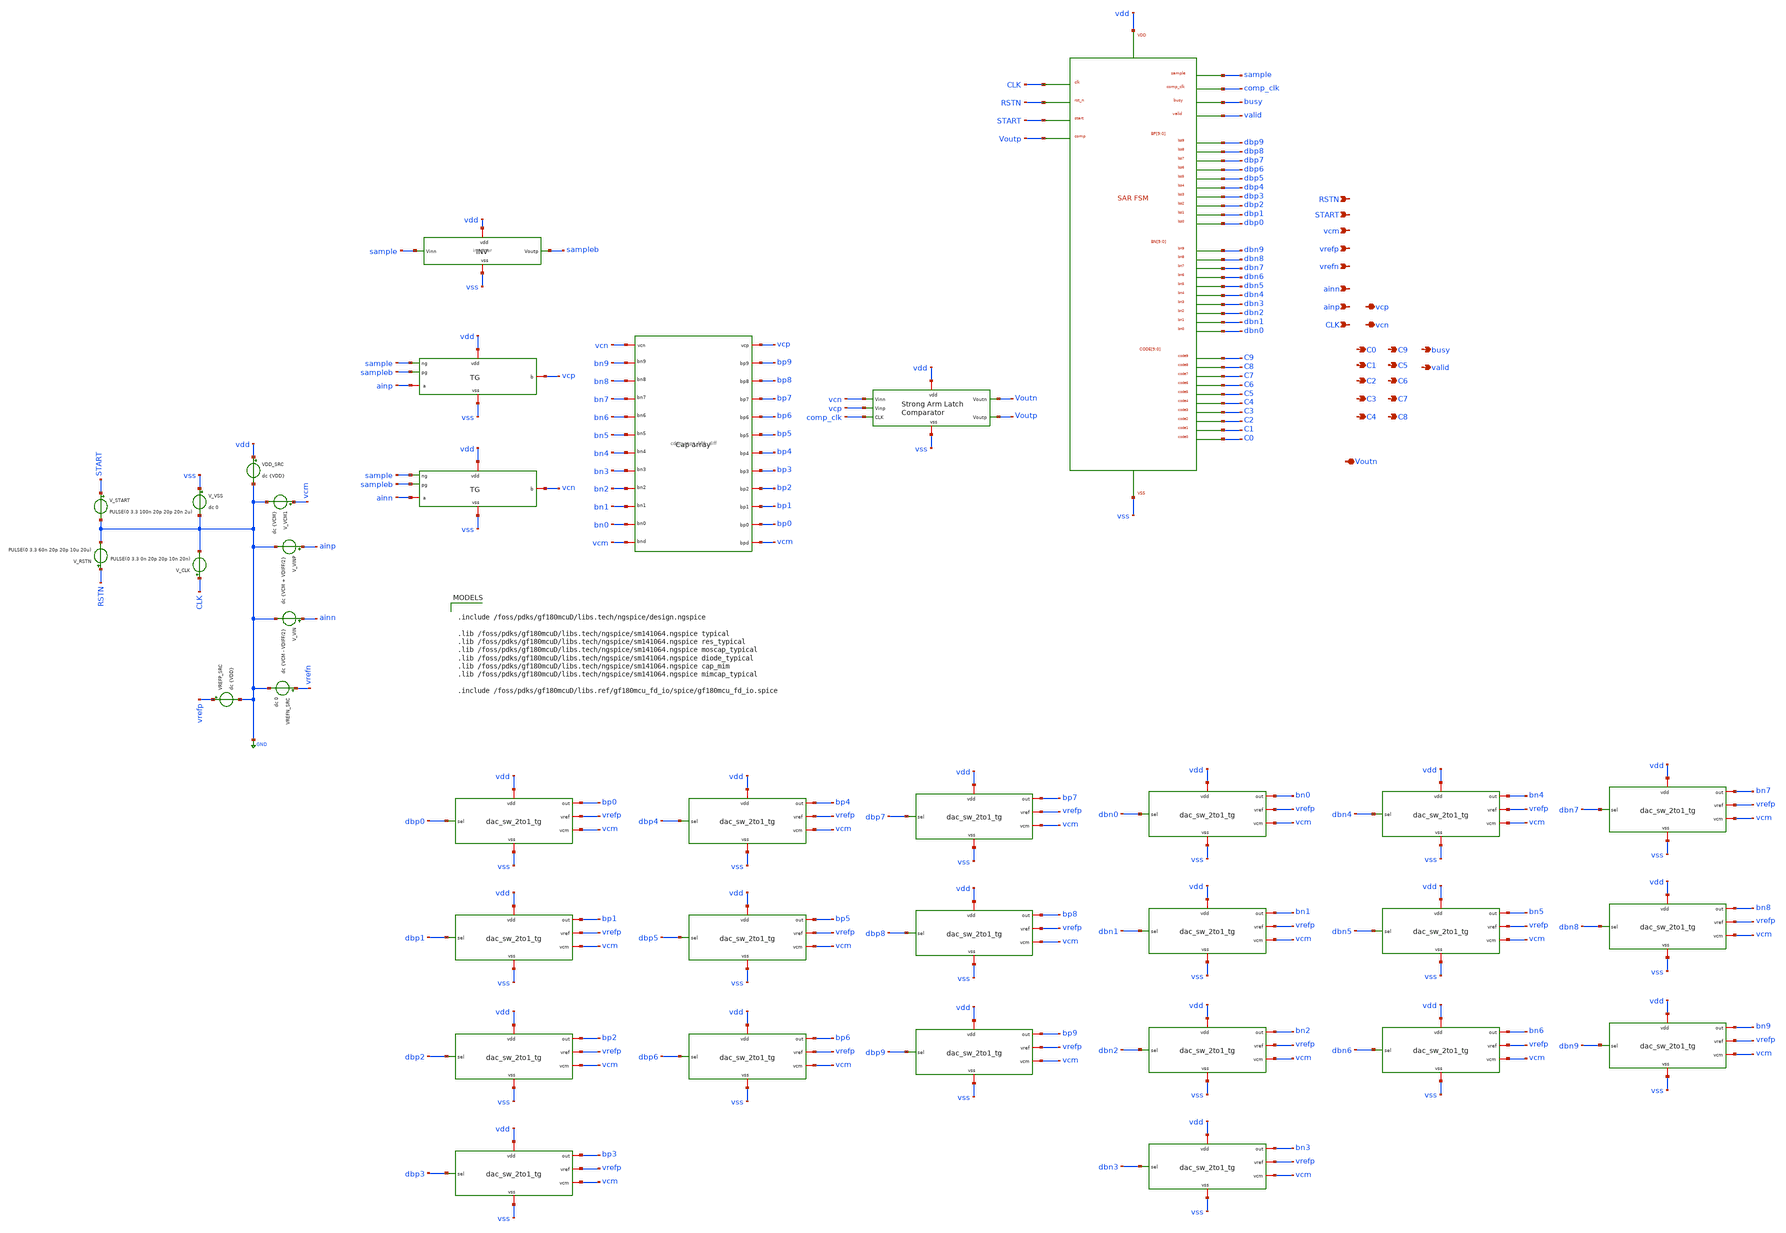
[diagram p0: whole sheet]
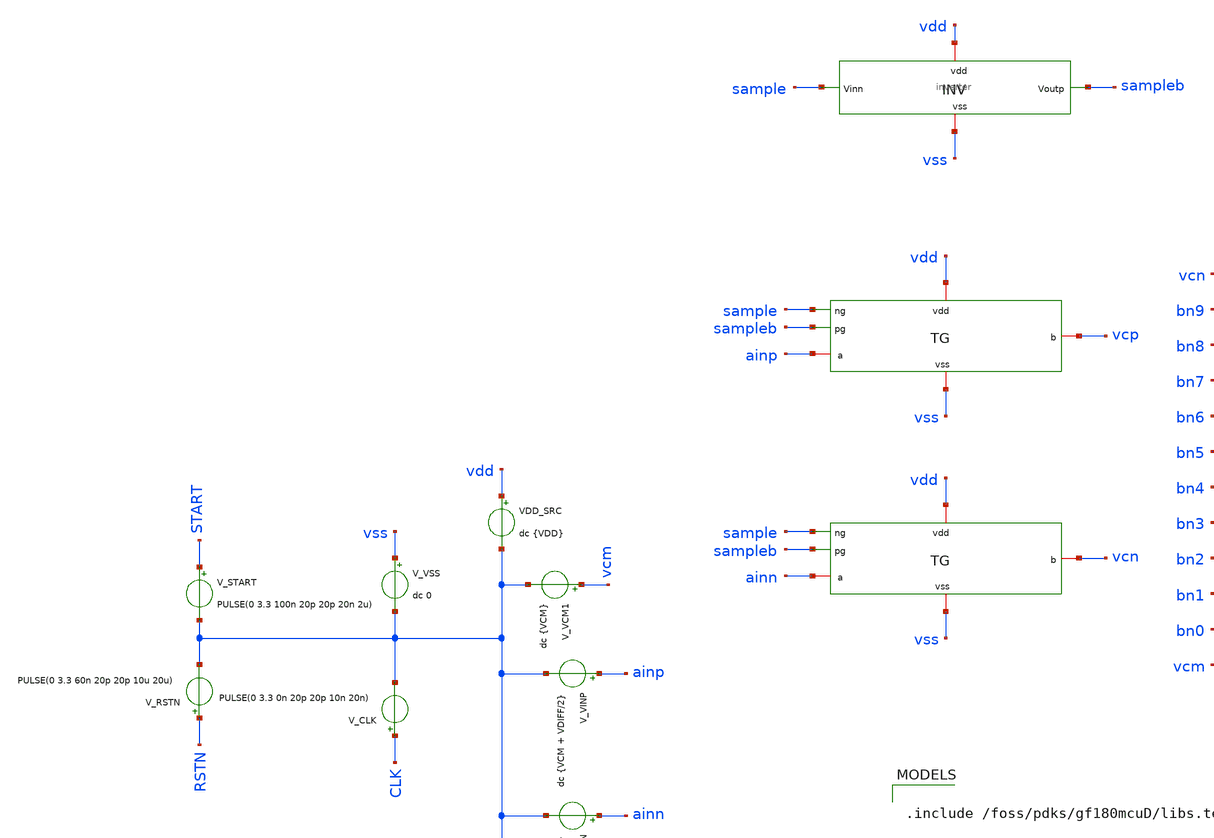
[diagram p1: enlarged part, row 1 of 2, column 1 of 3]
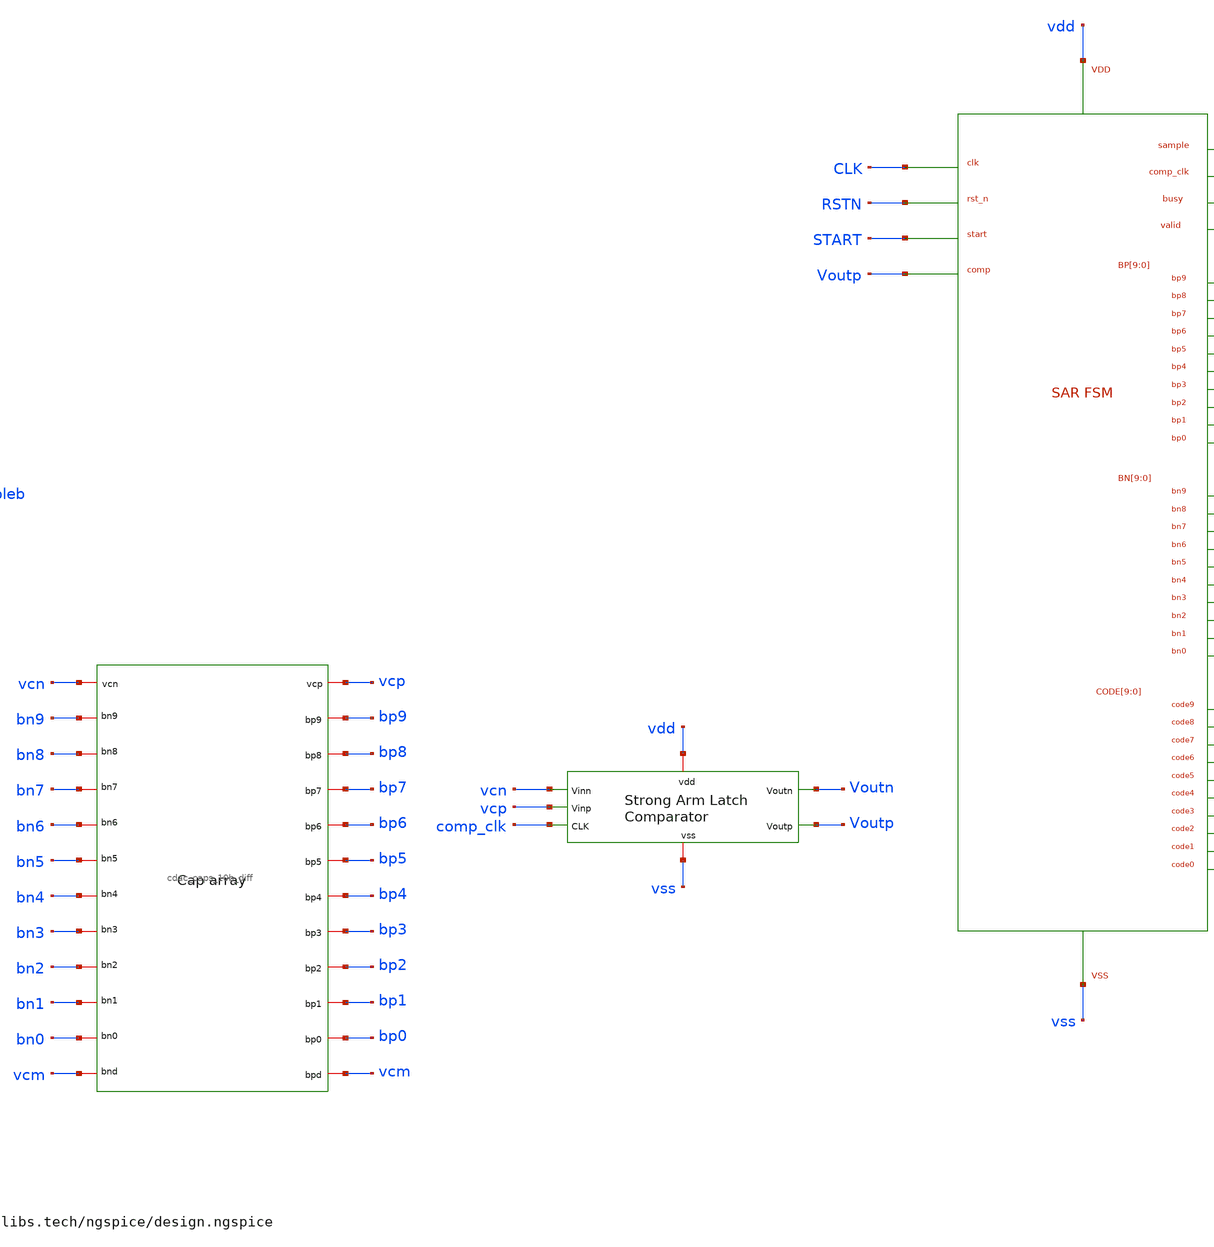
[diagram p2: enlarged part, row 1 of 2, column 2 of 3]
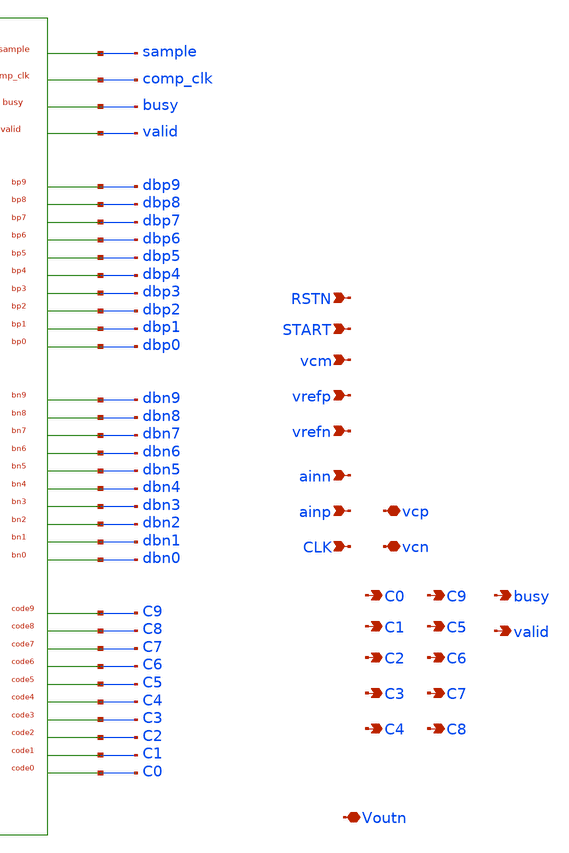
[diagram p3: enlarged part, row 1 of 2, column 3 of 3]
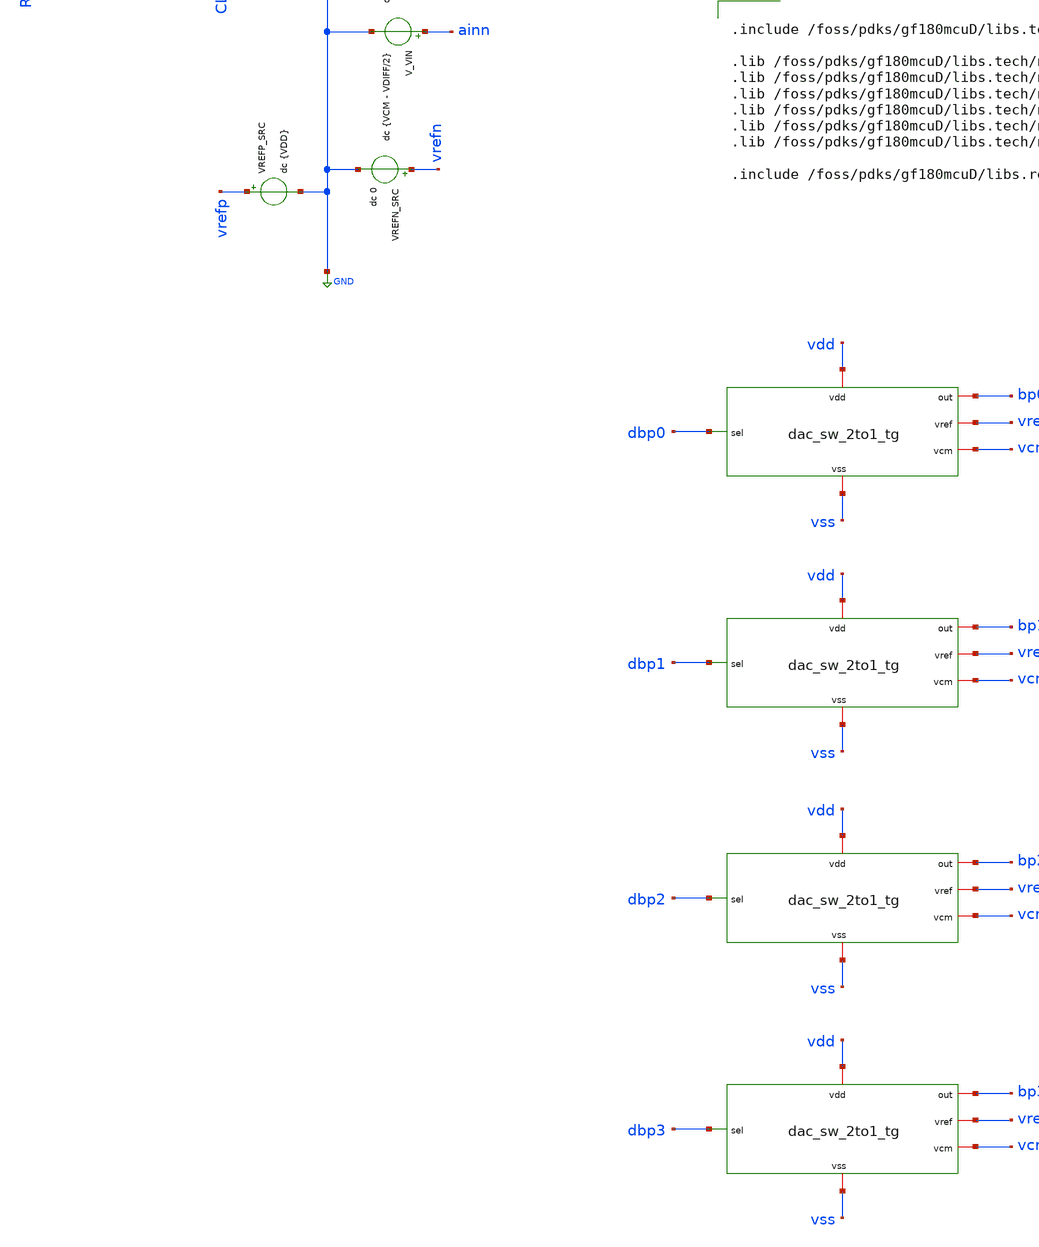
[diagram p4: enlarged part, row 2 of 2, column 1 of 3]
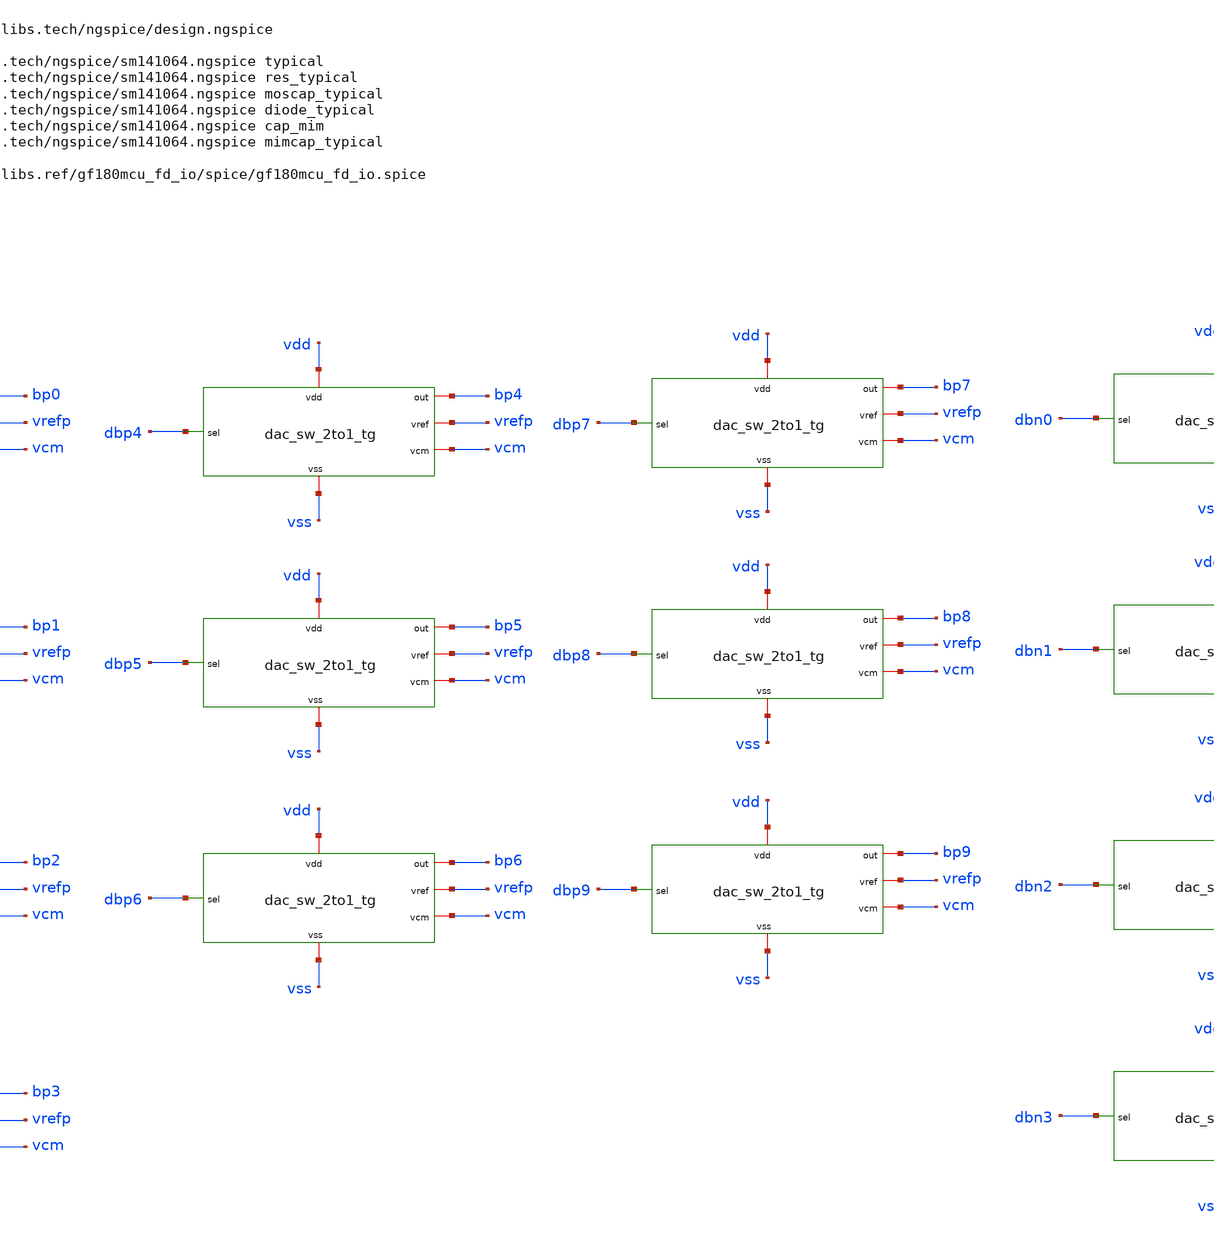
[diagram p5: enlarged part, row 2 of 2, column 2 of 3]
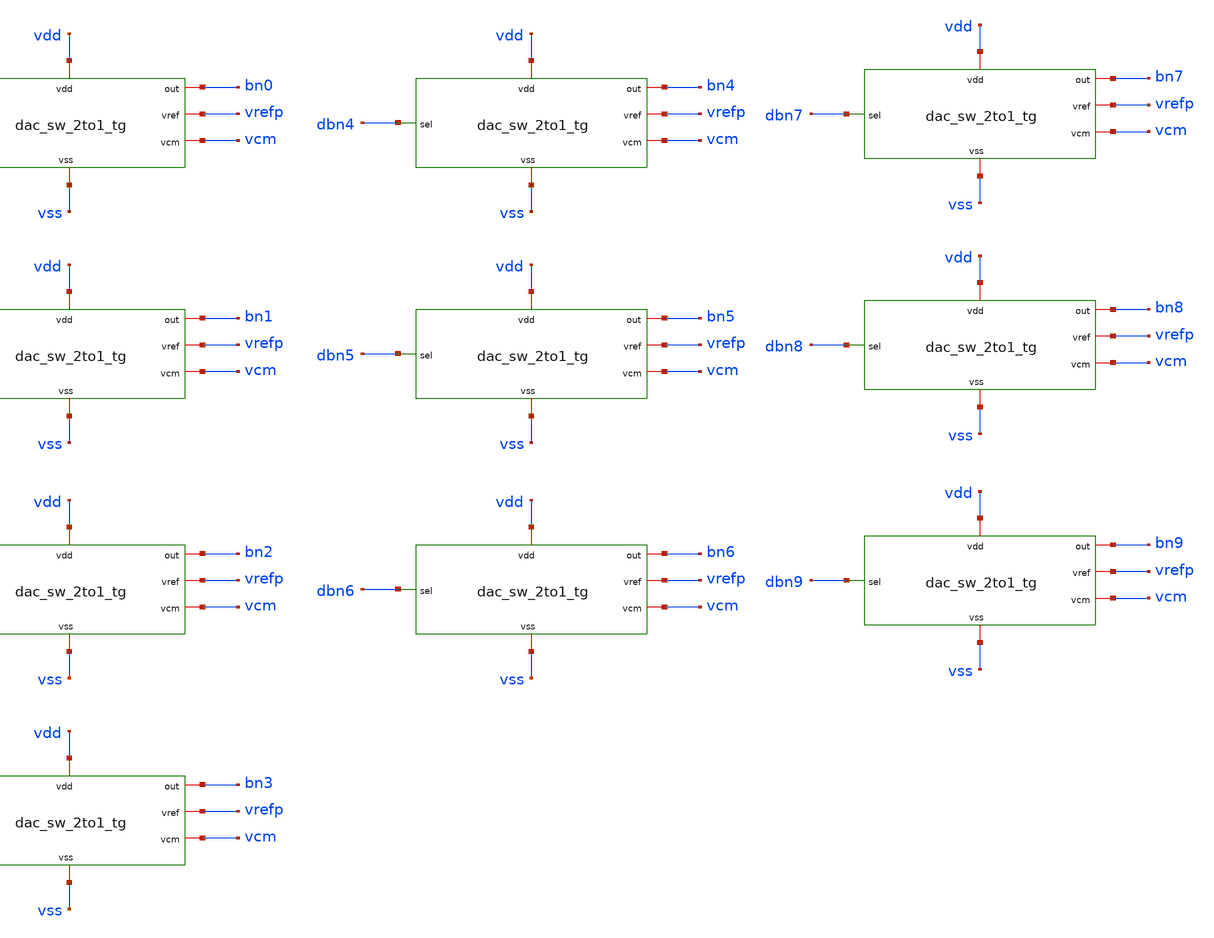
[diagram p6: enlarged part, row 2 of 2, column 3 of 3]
** sch_path: circuit_files/sar_adc_test/tb/cdac_comp_sar_fsm_tb.sch
**.subckt cdac_comp_sar_fsm_tb ainn vcp ainp CLK vcn vrefp vrefn vcm C1 C2 C3 C4 C5 C6 C7 C8 C0 C9
*+ busy valid START RSTN Voutn
*.ipin ainn
*.iopin vcp
*.ipin ainp
*.ipin CLK
*.iopin vcn
*.ipin vrefp
*.ipin vrefn
*.ipin vcm
*.opin C1
*.opin C2
*.opin C3
*.opin C4
*.opin C5
*.opin C6
*.opin C7
*.opin C8
*.opin C0
*.opin C9
*.opin busy
*.opin valid
*.ipin START
*.ipin RSTN
*.iopin Voutn
V_VIN ainn GND dc {VCM - VDIFF/2}
VDD_SRC vdd GND dc {VDD}
V_VINP ainp GND dc {VCM + VDIFF/2}
V_VSS vss GND dc 0
V_CLK CLK GND PULSE(0 3.3 0n 20p 20p 10n 20n)
x1 Voutn vcn Voutp vcp vdd vss comp_clk strong_arm_comp
x3 vss sample sampleb vdd ainp vcp tg
x4 vss sample sampleb vdd ainn vcn tg
V_VCM1 vcm GND dc {VCM}
x2 vcp bp3 bp0 bp5 bp2 vcm bp1 bp7 bp6 bp8 bp4 bp9 vcn bn0 bn1 bn8 bn7 bn6 bn5 bn4 bn3 bn9 bn2 vcm
+ cdac_caps_10b_diff
VREFN_SRC vrefn GND dc 0
VREFP_SRC vrefp GND dc {VDD}
V_RSTN RSTN GND PULSE(0 3.3 60n 20p 20p 10u 20u)
V_START START GND PULSE(0 3.3 100n 20p 20p 20n 2u)
x6 dbp0 bp0 vss vdd vrefp vcm dac_sw_2to1_tg
x7 dbp1 bp1 vss vdd vrefp vcm dac_sw_2to1_tg
x8 dbp4 bp4 vss vdd vrefp vcm dac_sw_2to1_tg
x9 dbp5 bp5 vss vdd vrefp vcm dac_sw_2to1_tg
x10 dbp7 bp7 vss vdd vrefp vcm dac_sw_2to1_tg
x11 dbp8 bp8 vss vdd vrefp vcm dac_sw_2to1_tg
x12 dbp2 bp2 vss vdd vrefp vcm dac_sw_2to1_tg
x13 dbp3 bp3 vss vdd vrefp vcm dac_sw_2to1_tg
x14 dbp6 bp6 vss vdd vrefp vcm dac_sw_2to1_tg
x16 dbp9 bp9 vss vdd vrefp vcm dac_sw_2to1_tg
x17 dbn0 bn0 vss vdd vrefp vcm dac_sw_2to1_tg
x18 dbn1 bn1 vss vdd vrefp vcm dac_sw_2to1_tg
x19 dbn4 bn4 vss vdd vrefp vcm dac_sw_2to1_tg
x20 dbn5 bn5 vss vdd vrefp vcm dac_sw_2to1_tg
x21 dbn7 bn7 vss vdd vrefp vcm dac_sw_2to1_tg
x22 dbn8 bn8 vss vdd vrefp vcm dac_sw_2to1_tg
x23 dbn2 bn2 vss vdd vrefp vcm dac_sw_2to1_tg
x24 dbn3 bn3 vss vdd vrefp vcm dac_sw_2to1_tg
x25 dbn6 bn6 vss vdd vrefp vcm dac_sw_2to1_tg
x27 dbn9 bn9 vss vdd vrefp vcm dac_sw_2to1_tg
x15 vdd sample sampleb vss inverter
x26 CLK RSTN START Voutp sample comp_clk busy valid dbp9 dbp8 dbp7 dbp6 dbp5 dbp4 dbp3 dbp2 dbp1
+ dbp0 dbn9 dbn8 dbn7 dbn6 dbn5 dbn4 dbn3 dbn2 dbn1 dbn0 C9 C8 C7 C6 C5 C4 C3 C2 C1 C0 vdd vss
+ sar_fsm_wrapper
**** begin user architecture code

.include /foss/pdks/gf180mcuD/libs.tech/ngspice/design.ngspice

.lib /foss/pdks/gf180mcuD/libs.tech/ngspice/sm141064.ngspice typical
.lib /foss/pdks/gf180mcuD/libs.tech/ngspice/sm141064.ngspice res_typical
.lib /foss/pdks/gf180mcuD/libs.tech/ngspice/sm141064.ngspice moscap_typical
.lib /foss/pdks/gf180mcuD/libs.tech/ngspice/sm141064.ngspice diode_typical
.lib /foss/pdks/gf180mcuD/libs.tech/ngspice/sm141064.ngspice cap_mim
.lib /foss/pdks/gf180mcuD/libs.tech/ngspice/sm141064.ngspice mimcap_typical

.include /foss/pdks/gf180mcuD/libs.ref/gf180mcu_fd_io/spice/gf180mcu_fd_io.spice



* ============================================================
* GF180 / SAR FSM + Comparator + CDAC mixed-signal testbench
* REAL DAC-switch version
* ============================================================

* Standard-cell SPICE and SAR FSM wrapper
.include /foss/pdks/gf180mcuD/libs.ref/gf180mcu_fd_sc_mcu7t5v0/spice/gf180mcu_fd_sc_mcu7t5v0.spice
.include /media/sf_LNA_chipathon/OCCPSense_Capacitive_Pressure_Sensor/rtl/sar_fsm/sar_fsm_wrapper_fixed.spice

* ------------------------------------------------------------
* Main parameters
* ------------------------------------------------------------
.param VDD=3.3
.param VCM=1.65
.param VDIFF=0.001611328125
.param WCU=5u
.param LCU=5u
.param COUT_LOAD=20f


* ============================================================
* SAR ADC POST-FIX SMALL RAMP DEBUG
* Dumps one row per VDIFF into:
*   sar_ramp_after_fix_results.txt
*
* Assumes current fixed schematic:
*   BP-side DAC vref pin -> vrefp
*   BN-side DAC vref pin -> vrefp
* ============================================================

.options reltol=1e-4 abstol=1e-12 vntol=1e-6
.options method=gear maxord=2
.options plotwinsize=0

* -----------------------------
* Save required nodes
* -----------------------------
.save v(CLK) v(RSTN) v(START)
.save v(sample) v(sampleb) v(comp_clk)
.save v(busy) v(valid)

.save v(ainp) v(ainn)
.save v(vcp) v(vcn)
.save v(vrefp) v(vrefn) v(vcm)
.save v(Voutp) v(Voutn)

.save v(C9) v(C8) v(C7) v(C6) v(C5)
.save v(C4) v(C3) v(C2) v(C1) v(C0)

.save v(dbp9) v(dbp8) v(dbp7) v(dbp6) v(dbp5)
.save v(dbp4) v(dbp3) v(dbp2) v(dbp1) v(dbp0)

.save v(dbn9) v(dbn8) v(dbn7) v(dbn6) v(dbn5)
.save v(dbn4) v(dbn3) v(dbn2) v(dbn1) v(dbn0)

.save v(bp9) v(bp8) v(bp7) v(bp6) v(bp5)
.save v(bp4) v(bp3) v(bp2) v(bp1) v(bp0)

.save v(bn9) v(bn8) v(bn7) v(bn6) v(bn5)
.save v(bn4) v(bn3) v(bn2) v(bn1) v(bn0)

.control

set noaskquit

shell rm -f sar_ramp_after_fix_results.txt

let logic_th = 1.65
let prev_code = -1
let run_index = 0
let monotonic_fail_count = 0

echo VDIFF VALID_SEEN T_DEBUG CODE C9 C8 C7 C6 C5 C4 C3 C2 C1 C0 VCP VCN VCP_MINUS_VCN VOUTP VOUTN
+ DBP9 DBP8 DBP7 DBP6 DBP5 DBP4 DBP3 DBP2 DBP1 DBP0 DBN9 DBN8 DBN7 DBN6 DBN5 DBN4 DBN3 DBN2 DBN1 DBN0 BP9
+ BP8 BP7 BP6 BP5 BP4 BP3 BP2 BP1 BP0 BN9 BN8 BN7 BN6 BN5 BN4 BN3 BN2 BN1 BN0 MONOTONIC_FAIL >
+ sar_ramp_after_fix_results.txt

* Small ramp around midscale.
foreach vdiff_val -0.020 -0.010 -0.005 -0.002 -0.001 0 0.001 0.001611328125 0.002 0.005 0.010 0.020

  alterparam VDIFF = $vdiff_val
  reset

  tran 20p 1.6u

  meas tran valid_max MAX v(valid) FROM=0n TO=1.6u

  let valid_seen = 0
  if valid_max > logic_th
    let valid_seen = 1
  end

  let t_debug = 1.55u
  if valid_seen > 0.5
    meas tran t_valid WHEN v(valid)=1.65 RISE=1
    let t_debug = t_valid + 5n
  end

  * -----------------------------
  * Code bits at debug time
  * -----------------------------
  meas tran c9v FIND v(C9) AT=$&t_debug
  meas tran c8v FIND v(C8) AT=$&t_debug
  meas tran c7v FIND v(C7) AT=$&t_debug
  meas tran c6v FIND v(C6) AT=$&t_debug
  meas tran c5v FIND v(C5) AT=$&t_debug
  meas tran c4v FIND v(C4) AT=$&t_debug
  meas tran c3v FIND v(C3) AT=$&t_debug
  meas tran c2v FIND v(C2) AT=$&t_debug
  meas tran c1v FIND v(C1) AT=$&t_debug
  meas tran c0v FIND v(C0) AT=$&t_debug

  let b9 = 0
  if c9v > logic_th
    let b9 = 1
  end

  let b8 = 0
  if c8v > logic_th
    let b8 = 1
  end

  let b7 = 0
  if c7v > logic_th
    let b7 = 1
  end

  let b6 = 0
  if c6v > logic_th
    let b6 = 1
  end

  let b5 = 0
  if c5v > logic_th
    let b5 = 1
  end

  let b4 = 0
  if c4v > logic_th
    let b4 = 1
  end

  let b3 = 0
  if c3v > logic_th
    let b3 = 1
  end

  let b2 = 0
  if c2v > logic_th
    let b2 = 1
  end

  let b1 = 0
  if c1v > logic_th
    let b1 = 1
  end

  let b0 = 0
  if c0v > logic_th
    let b0 = 1
  end

  let adc_code = 512*b9 + 256*b8 + 128*b7 + 64*b6 + 32*b5 + 16*b4 + 8*b3 + 4*b2 + 2*b1 + b0

  * -----------------------------
  * Analog values
  * -----------------------------
  meas tran vcpv   FIND v(vcp)   AT=$&t_debug
  meas tran vcnv   FIND v(vcn)   AT=$&t_debug
  meas tran voutpv FIND v(Voutp) AT=$&t_debug
  meas tran voutnv FIND v(Voutn) AT=$&t_debug

  let vdiff_cdac = vcpv - vcnv

  * -----------------------------
  * SAR DAC digital controls
  * -----------------------------
  meas tran dbp9v FIND v(dbp9) AT=$&t_debug
  meas tran dbp8v FIND v(dbp8) AT=$&t_debug
  meas tran dbp7v FIND v(dbp7) AT=$&t_debug
  meas tran dbp6v FIND v(dbp6) AT=$&t_debug
  meas tran dbp5v FIND v(dbp5) AT=$&t_debug
  meas tran dbp4v FIND v(dbp4) AT=$&t_debug
  meas tran dbp3v FIND v(dbp3) AT=$&t_debug
  meas tran dbp2v FIND v(dbp2) AT=$&t_debug
  meas tran dbp1v FIND v(dbp1) AT=$&t_debug
  meas tran dbp0v FIND v(dbp0) AT=$&t_debug

  meas tran dbn9v FIND v(dbn9) AT=$&t_debug
  meas tran dbn8v FIND v(dbn8) AT=$&t_debug
  meas tran dbn7v FIND v(dbn7) AT=$&t_debug
  meas tran dbn6v FIND v(dbn6) AT=$&t_debug
  meas tran dbn5v FIND v(dbn5) AT=$&t_debug
  meas tran dbn4v FIND v(dbn4) AT=$&t_debug
  meas tran dbn3v FIND v(dbn3) AT=$&t_debug
  meas tran dbn2v FIND v(dbn2) AT=$&t_debug
  meas tran dbn1v FIND v(dbn1) AT=$&t_debug
  meas tran dbn0v FIND v(dbn0) AT=$&t_debug

  * -----------------------------
  * Actual CDAC bottom plates
  * -----------------------------
  meas tran bp9v FIND v(bp9) AT=$&t_debug
  meas tran bp8v FIND v(bp8) AT=$&t_debug
  meas tran bp7v FIND v(bp7) AT=$&t_debug
  meas tran bp6v FIND v(bp6) AT=$&t_debug
  meas tran bp5v FIND v(bp5) AT=$&t_debug
  meas tran bp4v FIND v(bp4) AT=$&t_debug
  meas tran bp3v FIND v(bp3) AT=$&t_debug
  meas tran bp2v FIND v(bp2) AT=$&t_debug
  meas tran bp1v FIND v(bp1) AT=$&t_debug
  meas tran bp0v FIND v(bp0) AT=$&t_debug

  meas tran bn9v FIND v(bn9) AT=$&t_debug
  meas tran bn8v FIND v(bn8) AT=$&t_debug
  meas tran bn7v FIND v(bn7) AT=$&t_debug
  meas tran bn6v FIND v(bn6) AT=$&t_debug
  meas tran bn5v FIND v(bn5) AT=$&t_debug
  meas tran bn4v FIND v(bn4) AT=$&t_debug
  meas tran bn3v FIND v(bn3) AT=$&t_debug
  meas tran bn2v FIND v(bn2) AT=$&t_debug
  meas tran bn1v FIND v(bn1) AT=$&t_debug
  meas tran bn0v FIND v(bn0) AT=$&t_debug

  * -----------------------------
  * Monotonic check
  * -----------------------------
  let monotonic_fail = 0
  if run_index > 0
    if adc_code < prev_code
      let monotonic_fail = 1
      let monotonic_fail_count = monotonic_fail_count + 1
    end
  end

  echo $vdiff_val $&valid_seen $&t_debug $&adc_code $&b9 $&b8 $&b7 $&b6 $&b5 $&b4 $&b3 $&b2 $&b1
+ $&b0 $&vcpv $&vcnv $&vdiff_cdac $&voutpv $&voutnv $&dbp9v $&dbp8v $&dbp7v $&dbp6v $&dbp5v $&dbp4v
+ $&dbp3v $&dbp2v $&dbp1v $&dbp0v $&dbn9v $&dbn8v $&dbn7v $&dbn6v $&dbn5v $&dbn4v $&dbn3v $&dbn2v $&dbn1v
+ $&dbn0v $&bp9v $&bp8v $&bp7v $&bp6v $&bp5v $&bp4v $&bp3v $&bp2v $&bp1v $&bp0v $&bn9v $&bn8v $&bn7v $&bn6v
+ $&bn5v $&bn4v $&bn3v $&bn2v $&bn1v $&bn0v $&monotonic_fail >> sar_ramp_after_fix_results.txt

  let prev_code = adc_code
  let run_index = run_index + 1

end

echo ================================================== >> sar_ramp_after_fix_results.txt
echo RAMP_SUMMARY >> sar_ramp_after_fix_results.txt
echo number_of_points = $&run_index >> sar_ramp_after_fix_results.txt
echo monotonic_fail_count = $&monotonic_fail_count >> sar_ramp_after_fix_results.txt
echo Expected_after_fix: code should move monotonically with VDIFF. >>
+ sar_ramp_after_fix_results.txt
echo Near VDIFF=0, code should be close to 511 or 512. >> sar_ramp_after_fix_results.txt
echo ================================================== >> sar_ramp_after_fix_results.txt

echo ==================================================
echo SAR post-fix ramp test complete.
echo Results written to sar_ramp_after_fix_results.txt
echo ==================================================

.endc



**** end user architecture code
**.ends

* expanding   symbol:  strong_arm_comp.sym # of pins=7
** sym_path: circuit_files/sar_adc_test/xschem/strong_arm_comp.sym
** sch_path: circuit_files/sar_adc_test/xschem/strong_arm_comp.sch
.subckt strong_arm_comp Voutn Vinn Voutp Vinp vdd vss CLK
*.ipin Vinn
*.opin Voutp
*.iopin vdd
*.ipin Vinp
*.ipin CLK
*.iopin vss
*.opin Voutn
XM1 P CLK vdd vdd sg13_hv_pmos w=2u l=0.4u ng=1 m=4 mm_ok=1
XM2 net1 CLK vss vss sg13_hv_nmos w=2u l=0.45u ng=1 m=8 mm_ok=1
XM3 X CLK vdd vdd sg13_hv_pmos w=2u l=0.4u ng=1 m=4 mm_ok=1
XM4 P Vinn net1 vss sg13_hv_nmos w=2u l=0.45u ng=1 m=6 mm_ok=1
XM5 Q Vinp net1 vss sg13_hv_nmos w=2u l=0.45u ng=1 m=6 mm_ok=1
XM6 X Y P vss sg13_hv_nmos w=2u l=0.45u ng=1 m=2 mm_ok=1
XM7 Y X Q vss sg13_hv_nmos w=2u l=0.45u ng=1 m=2 mm_ok=1
XM8 X Y vdd vdd sg13_hv_pmos w=2u l=0.4u ng=1 m=4 mm_ok=1
XM9 Y CLK vdd vdd sg13_hv_pmos w=2u l=0.4u ng=1 m=4 mm_ok=1
XM10 Q CLK vdd vdd sg13_hv_pmos w=2u l=0.4u ng=1 m=4 mm_ok=1
XM11 Y X vdd vdd sg13_hv_pmos w=2u l=0.4u ng=1 m=4 mm_ok=1
XM12 net2 X vss vss sg13_hv_nmos w=2u l=0.45u ng=1 m=1 mm_ok=1
XM13 Voutp net2 vss vss sg13_hv_nmos w=2u l=0.45u ng=1 m=2 mm_ok=1
XM14 Voutn net3 vss vss sg13_hv_nmos w=2u l=0.45u ng=1 m=2 mm_ok=1
XM15 net3 Y vss vss sg13_hv_nmos w=2u l=0.45u ng=1 m=1 mm_ok=1
XM16 net2 X vdd vdd sg13_hv_pmos w=2u l=0.4u ng=1 m=2 mm_ok=1
XM17 Voutp Voutn vdd vdd sg13_hv_pmos w=2u l=0.4u ng=1 m=4 mm_ok=1
XM18 net3 Y vdd vdd sg13_hv_pmos w=2u l=0.4u ng=1 m=2 mm_ok=1
XM19 Voutn Voutp vdd vdd sg13_hv_pmos w=2u l=0.4u ng=1 m=4 mm_ok=1
.ends


* expanding   symbol:  tg.sym # of pins=6
** sym_path: circuit_files/sar_adc_test/xschem/tg.sym
** sch_path: circuit_files/sar_adc_test/xschem/tg.sch
.subckt tg vss ng pg vdd a b
*.ipin ng
*.iopin vdd
*.ipin pg
*.iopin a
*.iopin b
*.iopin vss
XM12 b ng a vss sg13_hv_nmos w=2u l=0.45u ng=1 m=1 mm_ok=1
XM16 b pg a vdd sg13_hv_pmos w=2u l=0.4u ng=1 m=2 mm_ok=1
.ends


* expanding   symbol:  cdac_caps_10b_diff.sym # of pins=24
** sym_path: circuit_files/sar_adc_test/xschem/cdac_caps_10b_diff.sym
** sch_path: circuit_files/sar_adc_test/xschem/cdac_caps_10b_diff.sch
.subckt cdac_caps_10b_diff vcp bp3 bp0 bp5 bp2 bpd bp1 bp7 bp6 bp8 bp4 bp9 vcn bn0 bn1 bn8 bn7 bn6
+ bn5 bn4 bn3 bn9 bn2 bnd
*.iopin vcp
*.iopin vcn
*.iopin bpd
*.iopin bp0
*.iopin bp1
*.iopin bp2
*.iopin bp3
*.iopin bp4
*.iopin bp5
*.iopin bp6
*.iopin bp7
*.iopin bp8
*.iopin bp9
*.iopin bnd
*.iopin bn1
*.iopin bn2
*.iopin bn3
*.iopin bn4
*.iopin bn5
*.iopin bn6
*.iopin bn7
*.iopin bn8
*.iopin bn9
*.iopin bn0
C2 vcp bp0 {1*Cu} m=1
C1 vcp bpd {1*Cu} m=1
C3 vcp bp2 {4*Cu} m=1
C4 vcp bp1 {2*Cu} m=1
C5 vcp bp5 {32*Cu} m=1
C6 vcp bp4 {16*Cu} m=1
C7 vcp bp7 {128*Cu} m=1
C8 vcp bp6 {64*Cu} m=1
C9 vcp bp8 {256*Cu} m=1
C10 vcp bp3 {8*Cu} m=1
C12 vcp bp9 {512*Cu} m=1
C11 vcn bn0 {1*Cu} m=1
C13 vcn bnd {1*Cu} m=1
C14 vcn bn2 {4*Cu} m=1
C15 vcn bn1 {2*Cu} m=1
C16 vcn bn5 {32*Cu} m=1
C17 vcn bn4 {16*Cu} m=1
C18 vcn bn7 {128*Cu} m=1
C19 vcn bn6 {64*Cu} m=1
C20 vcn bn8 {256*Cu} m=1
C21 vcn bn3 {8*Cu} m=1
C22 vcn bn9 {512*Cu} m=1
.ends


* expanding   symbol:  dac_sw_2to1_tg.sym # of pins=6
** sym_path: circuit_files/sar_adc_test/xschem/dac_sw_2to1_tg.sym
** sch_path: circuit_files/sar_adc_test/xschem/dac_sw_2to1_tg.sch
.subckt dac_sw_2to1_tg sel out vss vdd vref vcm
*.ipin sel
*.iopin vdd
*.iopin vref
*.iopin vcm
*.iopin vss
*.iopin out
x1 vss sel selb vdd vref out tg
x3 vss selb sel vdd vcm out tg
x2 vdd sel selb vss inverter
.ends


* expanding   symbol:  inverter.sym # of pins=4
** sym_path: circuit_files/sar_adc_test/xschem/inverter.sym
** sch_path: circuit_files/sar_adc_test/xschem/inverter.sch
.subckt inverter vdd Vinn Voutp vss
*.iopin vdd
*.iopin vss
*.ipin Vinn
*.opin Voutp
XM12 Voutp Vinn vss vss sg13_hv_nmos w=2u l=0.45u ng=1 m=1 mm_ok=1
XM16 Voutp Vinn vdd vdd sg13_hv_pmos w=2u l=0.4u ng=1 m=2 mm_ok=1
.ends


* expanding   symbol:  /media/sf_LNA_chipathon/sar_adc_gf180/src/sar_fsm/sar_fsm_wrapper.sym # of
*+ pins=40
** sym_path: circuit_files/src/sar_fsm/sar_fsm_wrapper.sym
.include /home/arjun/eda/projects/SAR_ADC/circuit_files/src/sar_fsm/build/sar_fsm_wrapper_ihp.spice
.GLOBAL GND
.end
